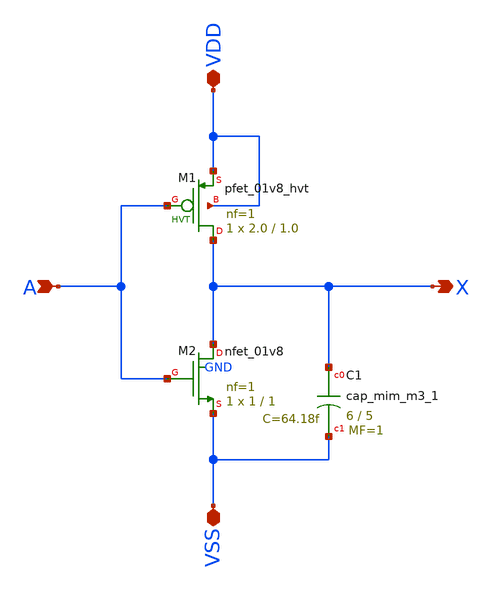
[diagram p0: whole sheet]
** sch_path: schem/inv_cap.sch
**.subckt inv_cap A X VDD VSS
*.ipin A
*.opin X
*.iopin VDD
*.iopin VSS
XM1 X A VDD VDD sky130_fd_pr__pfet_01v8_hvt L=1.0 W=2.0 nf=1 ad='int((1 + 1)/2) * 2.0 / 1 * 0.29' as='int((1 + 2)/2) * 2.0 / 1 * 0.29'
+ pd='2*int((1 + 1)/2) * (2.0 / 1 + 0.29)' ps='2*int((1 + 2)/2) * (2.0 / 1 + 0.29)' nrd='0.29 / 2.0 ' nrs='0.29 / 2.0 '
+ sa=0 sb=0 sd=0 mult=1 m=1
XM2 X A VSS GND sky130_fd_pr__nfet_01v8 L=1 W=1 nf=1 ad='int((1 + 1)/2) * 1 / 1 * 0.29' as='int((1 + 2)/2) * 1 / 1 * 0.29'
+ pd='2*int((1 + 1)/2) * (1 / 1 + 0.29)' ps='2*int((1 + 2)/2) * (1 / 1 + 0.29)' nrd='0.29 / 1 ' nrs='0.29 / 1 '
+ sa=0 sb=0 sd=0 mult=1 m=1
XC1 X VSS sky130_fd_pr__cap_mim_m3_1 W=6 L=5 MF=1 m=1
**.ends
.end
